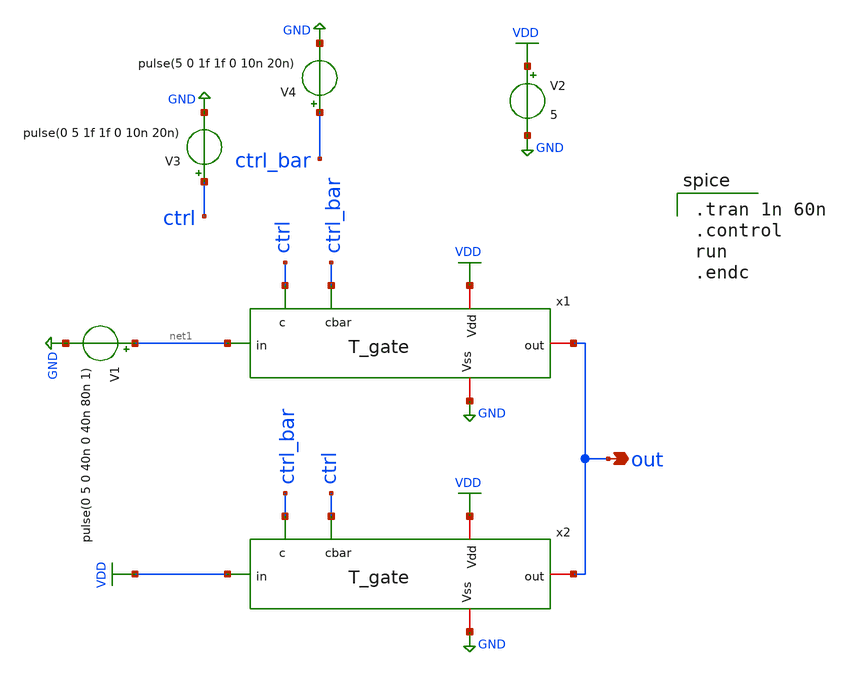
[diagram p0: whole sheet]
** sch_path: ADC/16bit_C2C/MagicAndSpice/T_gate_SPDT_TB.sch
**.subckt T_gate_SPDT_TB out
*.opin out
V1 net1 GND pulse(0 5 0 40n 0 40n 80n 1)
V2 VDD GND 5
V3 ctrl GND pulse(0 5 1f 1f 0 10n 20n)
V4 ctrl_bar GND pulse(5 0 1f 1f 0 10n 20n)
x1 ctrl out net1 VDD ctrl_bar GND T_gate
x2 ctrl_bar out VDD VDD ctrl GND T_gate
**** begin user architecture code

** opencircuitdesign pdks install
.lib $::SKYWATER_MODELS/sky130.lib.spice tt



.tran 1n 60n
.control
run
.endc

**** end user architecture code
**.ends

* expanding   symbol:  /home/ee431/workspace/6SAR_CDAC/T_gate.sym # of pins=6
** sym_path: ADC/16bit_C2C/MagicAndSpice/T_gate.sym
** sch_path: ADC/16bit_C2C/MagicAndSpice/T_gate.sch
.subckt T_gate c out in Vdd cbar Vss
*.ipin in
*.ipin cbar
*.ipin c
*.iopin Vdd
*.iopin Vss
*.iopin out
XM1 in c out GND sky130_fd_pr__nfet_g5v0d10v5 L=1 W=10 nf=1 ad='int((nf+1)/2) * W/nf * 0.29' as='int((nf+2)/2) * W/nf * 0.29'
+ pd='2*int((nf+1)/2) * (W/nf + 0.29)' ps='2*int((nf+2)/2) * (W/nf + 0.29)' nrd='0.29 / W' nrs='0.29 / W'
+ sa=0 sb=0 sd=0 mult=1 m=1
XM2 out cbar in Vdd sky130_fd_pr__pfet_g5v0d10v5 L=1 W=10 nf=1 ad='int((nf+1)/2) * W/nf * 0.29' as='int((nf+2)/2) * W/nf * 0.29'
+ pd='2*int((nf+1)/2) * (W/nf + 0.29)' ps='2*int((nf+2)/2) * (W/nf + 0.29)' nrd='0.29 / W' nrs='0.29 / W'
+ sa=0 sb=0 sd=0 mult=1 m=1
.ends

.GLOBAL GND
.GLOBAL VDD
.end
